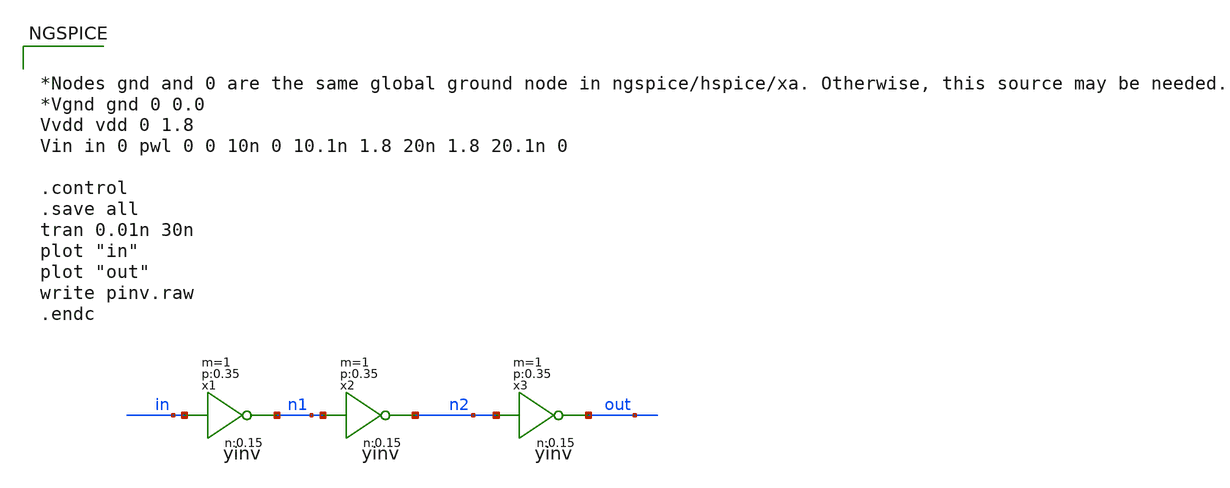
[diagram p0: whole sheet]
** sch_path: skywater-tests/inv_chain.sch
**.subckt inv_chain
x1 in n1 vdd gnd yinv W_N=1 L_N=0.15 W_P=2 L_P=0.35 m=1
x2 n1 n2 vdd gnd yinv W_N=1 L_N=0.15 W_P=2 L_P=0.35 m=1
x3 n2 out vdd gnd yinv W_N=1 L_N=0.15 W_P=2 L_P=0.35 m=1
**** begin user architecture code

.include $::SKYWATER_MODELS/cells/nfet_01v8/sky130_fd_pr__nfet_01v8__tt.corner.spice
.include $::SKYWATER_MODELS/cells/pfet_01v8/sky130_fd_pr__pfet_01v8__tt.corner.spice
* Mismatch parameters
.include $::SKYWATER_MODELS/cells/nfet_01v8/sky130_fd_pr__nfet_01v8__mismatch.corner.spice
.include $::SKYWATER_MODELS/cells/pfet_01v8/sky130_fd_pr__pfet_01v8__mismatch.corner.spice

* All models
.include $::SKYWATER_MODELS/models/all.spice



*Nodes gnd and 0 are the same global ground node in ngspice/hspice/xa. Otherwise, this source may be
*+ needed.
*Vgnd gnd 0 0.0
Vvdd vdd 0 1.8
Vin in 0 pwl 0 0 10n 0 10.1n 1.8 20n 1.8 20.1n 0

.control
.save all
tran 0.01n 30n
plot "in"
plot "out"
write pinv.raw
.endc


**** end user architecture code
**.ends

* expanding   symbol:  yinv.sym # of pins=2
** sym_path: skywater-tests/yinv.sym
** sch_path: skywater-tests/yinv.sch
.subckt yinv A Z VCCPIN VSSPIN     W_N=1 L_N=0.15 W_P=2 L_P=0.35
*.ipin A
*.opin Z
XM1 Z A VSSPIN VSSPIN sky130_fd_pr__nfet_01v8 L=L_N W=W_N nf=1 ad='int((nf+1)/2) * W/nf * 0.29' as='int((nf+2)/2) * W/nf * 0.29'
+ pd='2*int((nf+1)/2) * (W/nf + 0.29)' ps='2*int((nf+2)/2) * (W/nf + 0.29)' nrd='0.29 / W' nrs='0.29 / W'
+ sa=0 sb=0 sd=0 mult=1 m=1
XM2 Z A VCCPIN VCCPIN sky130_fd_pr__pfet_01v8 L=L_P W=W_P nf=1 ad='int((nf+1)/2) * W/nf * 0.29' as='int((nf+2)/2) * W/nf * 0.29'
+ pd='2*int((nf+1)/2) * (W/nf + 0.29)' ps='2*int((nf+2)/2) * (W/nf + 0.29)' nrd='0.29 / W' nrs='0.29 / W'
+ sa=0 sb=0 sd=0 mult=1 m=1
.ends

.end
